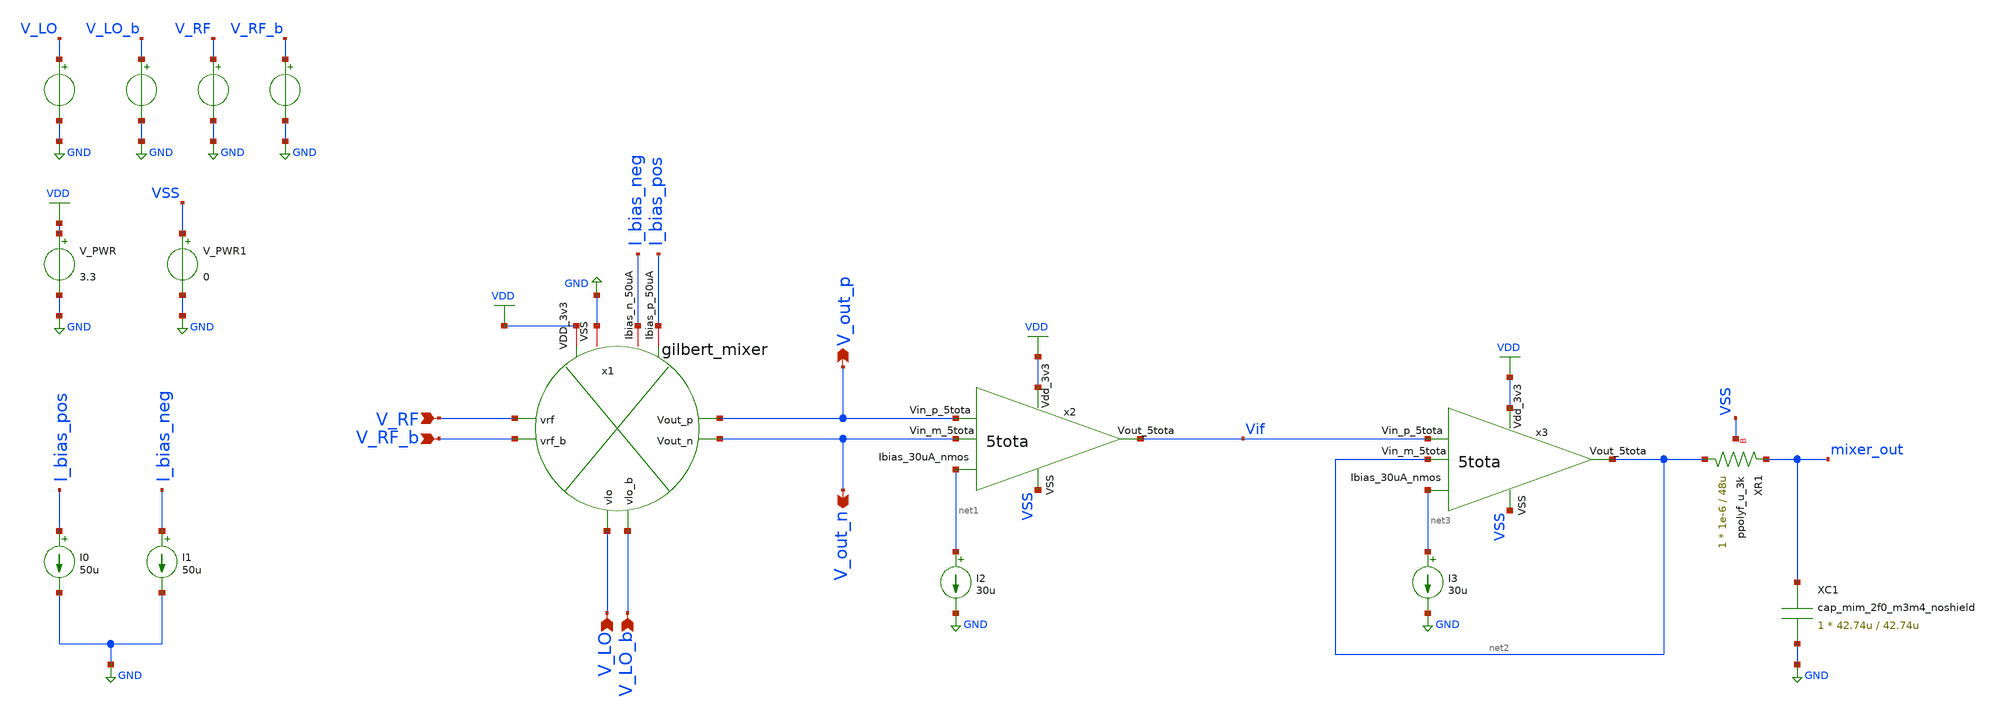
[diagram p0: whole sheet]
** sch_path: Analog/schematics/2_mixer/mixer_tb.sch
**.subckt mixer_tb V_LO V_LO_b V_RF V_RF_b V_out_p V_out_n
*.ipin V_LO
*.ipin V_LO_b
*.ipin V_RF
*.ipin V_RF_b
*.opin V_out_p
*.opin V_out_n
I2 net1 GND 30u
V_PWR VDD GND 3.3
.save i(v_pwr)
V_LO V_LO GND pulse(0 1.5 0 1p 1p 0.25n 0.5n)
.save i(v_lo)
V_LO_b V_LO_b GND pulse(0 1.5 0 1p 1p 0.25n 0.5n)
.save i(v_lo_b)
V_RF V_RF GND sin( 1 1 1 0 )
.save i(v_rf)
V_RF_b V_RF_b GND sin( 1 1 1 0 0 180 )
.save i(v_rf_b)
I0 I_bias_pos GND 50u
I1 I_bias_neg GND 50u
V_PWR1 VSS GND 0
.save i(v_pwr1)
x1 V_out_n V_out_p V_LO V_LO_b V_RF V_RF_b I_bias_neg I_bias_pos GND VDD gilbert_mixer
x2 VDD Vif V_out_p V_out_n VSS net1 5tota
x3 VDD net2 Vif net2 VSS net3 5tota
I3 net3 GND 30u
XC1 mixer_out GND cap_mim_2f0_m3m4_noshield c_width=42.74u c_length=42.74u m=1
XR1 net2 mixer_out VSS ppolyf_u_3k r_width=1e-6 r_length=48u m=1
**** begin user architecture code

.include $::180MCU_MODELS/design.ngspice
.lib $::180MCU_MODELS/sm141064.ngspice typical
.lib $::180MCU_MODELS/sm141064.ngspice mimcap_typical
.lib $::180MCU_MODELS/sm141064.ngspice cap_mim
.lib $::180MCU_MODELS/sm141064.ngspice res_typical




* let sets vectors to a plot, while set sets a variable, globally accessible in .control
.control

    * Set frequency and amplitude variables to proper values from within the control sequence
    * sine-wave LO
    * set cm_lo = 0.5
    * set freq_lo = 2.50G
    * set amp_lo = 0.5
    * alter @V_LO[sin] = [ $cm_lo $amp_lo $freq_lo 0 ]
    * alter @V_LO_b[sin] = [ $cm_lo $amp_lo $freq_lo 0 0 180 ]

    set freq_lo = 156k
    set cm_lo = 1.8
    set amp_lo = 0.4

    set cm_rf  = 1.2
    set freq_rf = 156k
    * set freq_rf = 10.7Meg
    set amp_rf  = 0.1

    * set the parameters to the voltage sources
    * alter @V_LO[pulse] = [ 2 2.5 0 0.5p 0.5p 5n 10n ]
    * alter @V_LO_b[pulse] = [ 2 2.5 5n 0.5p 0.5p 5n 10n]
    alter @V_LO[sin] = [ $cm_lo $amp_lo $freq_lo 0 ]
    alter @V_LO_b[sin] = [ $cm_lo $amp_lo $freq_lo 0 0 180 ]
    alter @V_RF[sin] = [ $cm_rf $amp_rf $freq_rf 0 ]
    alter @V_RF_b[sin] = [ $cm_rf $amp_rf $freq_rf 0 0 180 ]

    save all

    tran 10n 2m

    * 1. Define base differential vectors
    let if_out = v(v_out_p) - v(v_out_n)
    let vlo    = v(v_lo) - v(v_lo_b)
    let vrf    = v(v_rf) - v(v_rf_b)

    * 2. Linearize all signals onto a clean frequency grid
    linearize v(mixer_out) v(vif) vlo vrf

    * 3. Run the FFT across all active nodes at once
    fft v(mixer_out) v(vif) vlo vrf

    * 4. Compute unique, non-overlapping decibel variables
    let final_vlo_db  = db(mag(vlo))
    let final_vrf_db  = db(mag(vrf))
    let final_vif_db  = db(mag(v(vif)))
    let final_lpf_db  = db(mag(v(mixer_out)))

    * 5. SINGLE PLOT EXPRESSION: Plot the true, clean spectrum
    plot final_vlo_db final_vrf_db final_vif_db final_lpf_db xlimit 0 400k

    write /workspace/Analog/schematics/2_mixer/simulation_files/mixer_tb.raw

.endc


**** end user architecture code
**.ends
.GLOBAL GND
.GLOBAL VDD
.end
